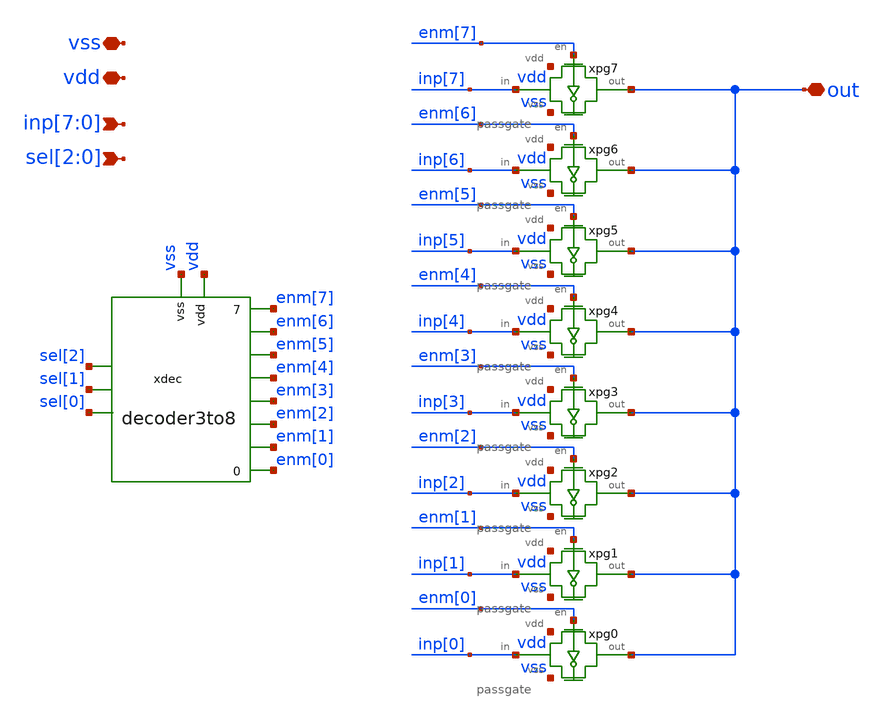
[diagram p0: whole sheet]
** sch_path: xschem/testbuffer/mux.sch
**.subckt mux out inp[7],inp[6],inp[5],inp[4],inp[3],inp[2],inp[1],inp[0] vss vdd
*+ sel[2],sel[1],sel[0]
*.iopin out
*.ipin inp[7],inp[6],inp[5],inp[4],inp[3],inp[2],inp[1],inp[0]
*.iopin vss
*.iopin vdd
*.ipin sel[2],sel[1],sel[0]
xpg1 out enm[1] vdd inp[1] vss passgate
xpg0 out enm[0] vdd inp[0] vss passgate
xpg3 out enm[3] vdd inp[3] vss passgate
xpg2 out enm[2] vdd inp[2] vss passgate
xpg5 out enm[5] vdd inp[5] vss passgate
xpg4 out enm[4] vdd inp[4] vss passgate
xpg6 out enm[6] vdd inp[6] vss passgate
xpg7 out enm[7] vdd inp[7] vss passgate
xdec enm[5] vdd vss enm[4] enm[3] enm[2] enm[1] enm[0] enm[6] enm[7] sel[0] sel[1] sel[2]
+ decoder3to8
**.ends

* expanding   symbol:  switches/passgate.sym # of pins=5
** sym_path: xschem/switches/passgate.sym
** sch_path: xschem/switches/passgate.sch
.subckt passgate out en vdd in vss
*.iopin out
*.ipin en
*.iopin vss
*.iopin vdd
*.iopin in
x2 vdd en enb vss inv_lvt
x1 vdd enb en_buf vss inv_lvt
XMSN out en_buf in vss sky130_fd_pr__nfet_01v8 L=0.5 W=1 nf=1 ad='int((nf+1)/2) * W/nf * 0.29' as='int((nf+2)/2) * W/nf * 0.29'
+ pd='2*int((nf+1)/2) * (W/nf + 0.29)' ps='2*int((nf+2)/2) * (W/nf + 0.29)' nrd='0.29 / W' nrs='0.29 / W'
+ sa=0 sb=0 sd=0 mult=1 m=1
XMSP in enb out vdd sky130_fd_pr__pfet_01v8 L=0.5 W=1 nf=1 ad='int((nf+1)/2) * W/nf * 0.29' as='int((nf+2)/2) * W/nf * 0.29'
+ pd='2*int((nf+1)/2) * (W/nf + 0.29)' ps='2*int((nf+2)/2) * (W/nf + 0.29)' nrd='0.29 / W' nrs='0.29 / W'
+ sa=0 sb=0 sd=0 mult=1 m=1
.ends


* expanding   symbol:  logic/inv_lvt.sym # of pins=4
** sym_path: xschem/logic/inv_lvt.sym
** sch_path: xschem/logic/inv_lvt.sch
.subckt inv_lvt vdd in out vss
*.iopin vdd
*.iopin vss
*.ipin in
*.opin out
XM1 out in vss vss sky130_fd_pr__nfet_01v8_lvt L=0.4 W=1 nf=1 ad='int((nf+1)/2) * W/nf * 0.29' as='int((nf+2)/2) * W/nf * 0.29'
+ pd='2*int((nf+1)/2) * (W/nf + 0.29)' ps='2*int((nf+2)/2) * (W/nf + 0.29)' nrd='0.29 / W' nrs='0.29 / W'
+ sa=0 sb=0 sd=0 mult=1 m=1
XM2 out in vdd vdd sky130_fd_pr__pfet_01v8_lvt L=0.4 W=1 nf=1 ad='int((nf+1)/2) * W/nf * 0.29' as='int((nf+2)/2) * W/nf * 0.29'
+ pd='2*int((nf+1)/2) * (W/nf + 0.29)' ps='2*int((nf+2)/2) * (W/nf + 0.29)' nrd='0.29 / W' nrs='0.29 / W'
+ sa=0 sb=0 sd=0 mult=1 m=1
.ends

.end
